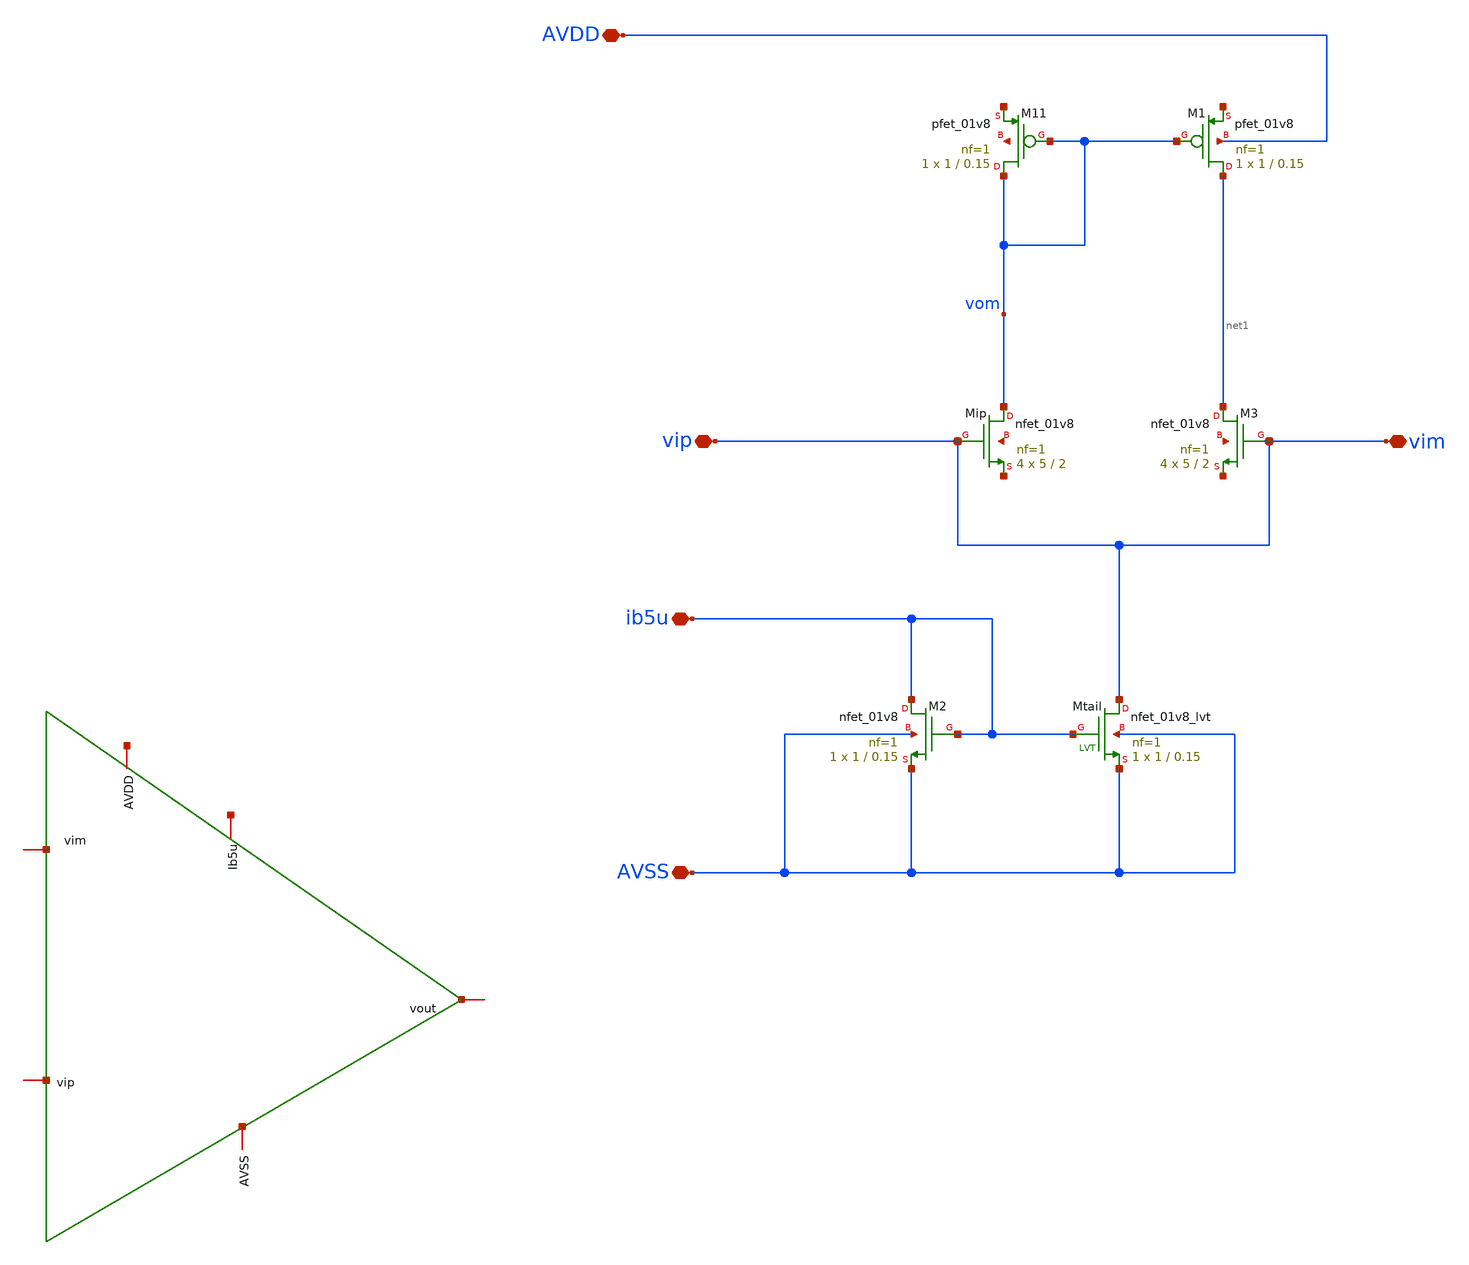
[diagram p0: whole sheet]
** sch_path: xschem/untitled-7.sch
**.subckt untitled-7 ib5u AVSS vim vip AVDD
*.iopin ib5u
*.iopin AVSS
*.iopin vim
*.iopin vip
*.iopin AVDD
XMtail vim ib5u AVSS AVSS sky130_fd_pr__nfet_01v8_lvt L=0.15 W=1 nf=1 ad='int((1 + 1)/2) * 1 / 1 * 0.29'
+ as='int((1 + 2)/2) * 1 / 1 * 0.29' pd='2*int((1 + 1)/2) * (1 / 1 + 0.29)' ps='2*int((1 + 2)/2) * (1 / 1 + 0.29)'
+ nrd='0.29 / 1 ' nrs='0.29 / 1 ' sa=0 sb=0 sd=0 mult=1 m=1
XM2 ib5u ib5u AVSS AVSS sky130_fd_pr__nfet_01v8 L=0.15 W=1 nf=1 ad='int((1 + 1)/2) * 1 / 1 * 0.29' as='int((1 + 2)/2) * 1 / 1 * 0.29'
+ pd='2*int((1 + 1)/2) * (1 / 1 + 0.29)' ps='2*int((1 + 2)/2) * (1 / 1 + 0.29)' nrd='0.29 / 1 ' nrs='0.29 / 1 '
+ sa=0 sb=0 sd=0 mult=1 m=1
XMip vom vim net2 net3 sky130_fd_pr__nfet_01v8 L=2 W=5 nf=1 ad='int((1 + 1)/2) * 5 / 1 * 0.29' as='int((1 + 2)/2) * 5 / 1 * 0.29'
+ pd='2*int((1 + 1)/2) * (5 / 1 + 0.29)' ps='2*int((1 + 2)/2) * (5 / 1 + 0.29)' nrd='0.29 / 5 ' nrs='0.29 / 5 '
+ sa=0 sb=0 sd=0 mult=4 m=4
XM3 net1 vim net4 net5 sky130_fd_pr__nfet_01v8 L=2 W=5 nf=1 ad='int((1 + 1)/2) * 5 / 1 * 0.29' as='int((1 + 2)/2) * 5 / 1 * 0.29'
+ pd='2*int((1 + 1)/2) * (5 / 1 + 0.29)' ps='2*int((1 + 2)/2) * (5 / 1 + 0.29)' nrd='0.29 / 5 ' nrs='0.29 / 5 '
+ sa=0 sb=0 sd=0 mult=4 m=4
XM11 vom vom net6 net7 sky130_fd_pr__pfet_01v8 L=0.15 W=1 nf=1 ad='int((nf+1)/2) * W/nf * 0.29' as='int((nf+2)/2) * W/nf * 0.29'
+ pd='2*int((nf+1)/2) * (W/nf + 0.29)' ps='2*int((nf+2)/2) * (W/nf + 0.29)' nrd='0.29 / W' nrs='0.29 / W'
+ sa=0 sb=0 sd=0 mult=1 m=1
XM1 net1 vom net8 AVDD sky130_fd_pr__pfet_01v8 L=0.15 W=1 nf=1 ad='int((nf+1)/2) * W/nf * 0.29' as='int((nf+2)/2) * W/nf * 0.29'
+ pd='2*int((nf+1)/2) * (W/nf + 0.29)' ps='2*int((nf+2)/2) * (W/nf + 0.29)' nrd='0.29 / W' nrs='0.29 / W'
+ sa=0 sb=0 sd=0 mult=1 m=1
**.ends
.end
